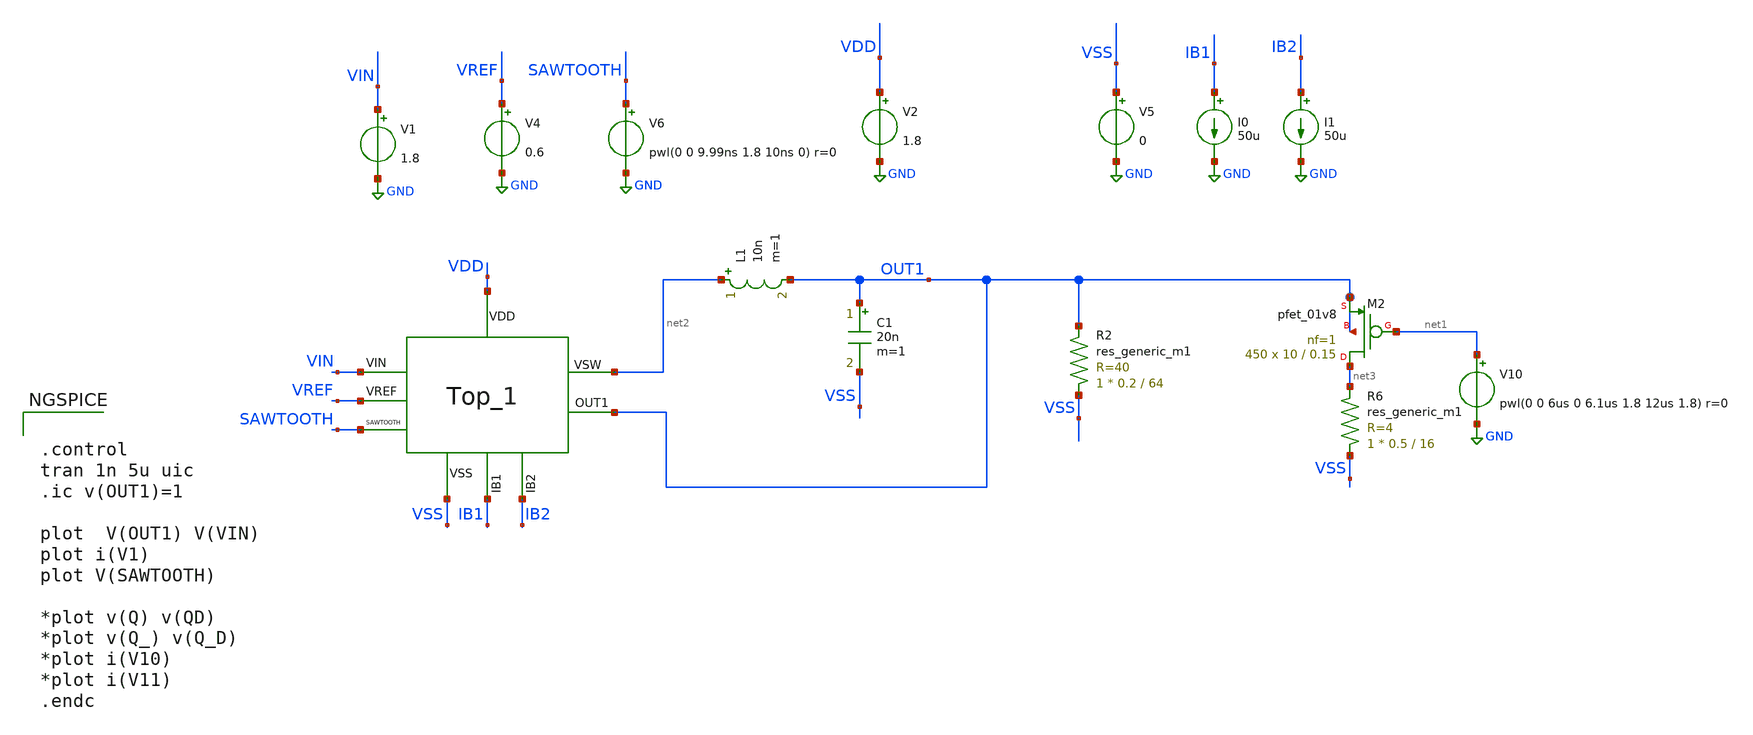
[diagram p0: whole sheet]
** sch_path: xschem/DC_DC_Converter_xschem/OTHERS/DC_DC_Converter_V7/TOP_LEVEL/Top_Final/Top_1_TB.sch
**.subckt Top_1_TB
V1 VIN GND 1.8
I0 IB1 GND 50u
V2 VDD GND 1.8
V5 VSS GND 0
V4 VREF GND 0.6
I1 IB2 GND 50u
V6 SAWTOOTH GND pwl(0 0 9.99ns 1.8 10ns 0) r=0
L1 net2 OUT1 10n m=1
C1 OUT1 VSS 20n m=1
XM2 net3 net1 OUT1 OUT1 sky130_fd_pr__pfet_01v8 L=0.15 W=10 nf=1 ad='int((nf+1)/2) * W/nf * 0.29' as='int((nf+2)/2) * W/nf * 0.29'
+ pd='2*int((nf+1)/2) * (W/nf + 0.29)' ps='2*int((nf+2)/2) * (W/nf + 0.29)' nrd='0.29 / W' nrs='0.29 / W'
+ sa=0 sb=0 sd=0 mult=450 m=450
V10 net1 GND pwl(0 0 6us 0 6.1us 1.8 12us 1.8) r=0
R2 VSS OUT1 sky130_fd_pr__res_generic_m1 W=0.2 L=64 m=1
R6 VSS net3 sky130_fd_pr__res_generic_m1 W=0.5 L=16 m=1
x2 VDD VIN OUT1 VREF SAWTOOTH IB2 IB1 VSS net2 Top_1
**** begin user architecture code

** opencircuitdesign pdks install
.lib $::SKYWATER_MODELS/sky130.lib.spice tt




.control
tran 1n 5u uic
.ic v(OUT1)=1

plot  V(OUT1) V(VIN)
plot i(V1)
plot V(SAWTOOTH)

*plot v(Q) v(QD)
*plot v(Q_) v(Q_D)
*plot i(V10)
*plot i(V11)
.endc


**** end user architecture code
**.ends
.GLOBAL GND
.end
